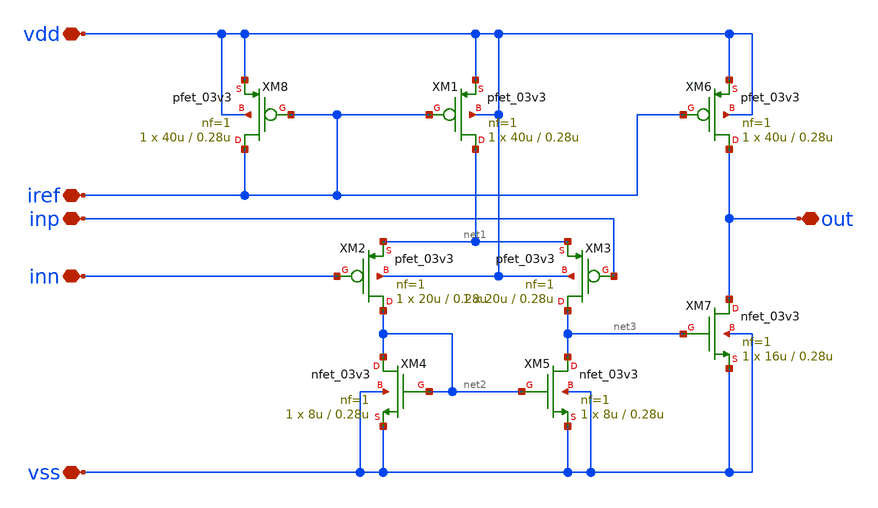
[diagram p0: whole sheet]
** sch_path: designs/libs/qw_core_analog_pkedit/PMOScomparator.sch
**.subckt PMOScomparator inp inn vdd vss out iref
*.iopin inp
*.iopin inn
*.iopin vdd
*.iopin vss
*.iopin out
*.iopin iref
XM8 iref iref vdd vdd pfet_03v3 L=0.28u W=40u nf=1 ad='int((nf+1)/2) * W/nf * 0.18u' as='int((nf+2)/2) * W/nf * 0.18u'
+ pd='2*int((nf+1)/2) * (W/nf + 0.18u)' ps='2*int((nf+2)/2) * (W/nf + 0.18u)' nrd='0.18u / W' nrs='0.18u / W'
+ sa=0 sb=0 sd=0 m=1
XM1 net1 iref vdd vdd pfet_03v3 L=0.28u W=40u nf=1 ad='int((nf+1)/2) * W/nf * 0.18u' as='int((nf+2)/2) * W/nf * 0.18u'
+ pd='2*int((nf+1)/2) * (W/nf + 0.18u)' ps='2*int((nf+2)/2) * (W/nf + 0.18u)' nrd='0.18u / W' nrs='0.18u / W'
+ sa=0 sb=0 sd=0 m=1
XM2 net2 inn net1 vdd pfet_03v3 L=0.28u W=20u nf=1 ad='int((nf+1)/2) * W/nf * 0.18u' as='int((nf+2)/2) * W/nf * 0.18u'
+ pd='2*int((nf+1)/2) * (W/nf + 0.18u)' ps='2*int((nf+2)/2) * (W/nf + 0.18u)' nrd='0.18u / W' nrs='0.18u / W'
+ sa=0 sb=0 sd=0 m=1
XM3 net3 inp net1 vdd pfet_03v3 L=0.28u W=20u nf=1 ad='int((nf+1)/2) * W/nf * 0.18u' as='int((nf+2)/2) * W/nf * 0.18u'
+ pd='2*int((nf+1)/2) * (W/nf + 0.18u)' ps='2*int((nf+2)/2) * (W/nf + 0.18u)' nrd='0.18u / W' nrs='0.18u / W'
+ sa=0 sb=0 sd=0 m=1
XM4 net2 net2 vss vss nfet_03v3 L=0.28u W=8u nf=1 ad='int((nf+1)/2) * W/nf * 0.18u' as='int((nf+2)/2) * W/nf * 0.18u'
+ pd='2*int((nf+1)/2) * (W/nf + 0.18u)' ps='2*int((nf+2)/2) * (W/nf + 0.18u)' nrd='0.18u / W' nrs='0.18u / W'
+ sa=0 sb=0 sd=0 m=1
XM5 net3 net2 vss vss nfet_03v3 L=0.28u W=8u nf=1 ad='int((nf+1)/2) * W/nf * 0.18u' as='int((nf+2)/2) * W/nf * 0.18u'
+ pd='2*int((nf+1)/2) * (W/nf + 0.18u)' ps='2*int((nf+2)/2) * (W/nf + 0.18u)' nrd='0.18u / W' nrs='0.18u / W'
+ sa=0 sb=0 sd=0 m=1
XM6 out iref vdd vdd pfet_03v3 L=0.28u W=40u nf=1 ad='int((nf+1)/2) * W/nf * 0.18u' as='int((nf+2)/2) * W/nf * 0.18u'
+ pd='2*int((nf+1)/2) * (W/nf + 0.18u)' ps='2*int((nf+2)/2) * (W/nf + 0.18u)' nrd='0.18u / W' nrs='0.18u / W'
+ sa=0 sb=0 sd=0 m=1
XM7 out net3 vss vss nfet_03v3 L=0.28u W=16u nf=1 ad='int((nf+1)/2) * W/nf * 0.18u' as='int((nf+2)/2) * W/nf * 0.18u'
+ pd='2*int((nf+1)/2) * (W/nf + 0.18u)' ps='2*int((nf+2)/2) * (W/nf + 0.18u)' nrd='0.18u / W' nrs='0.18u / W'
+ sa=0 sb=0 sd=0 m=1
**.ends
.end
